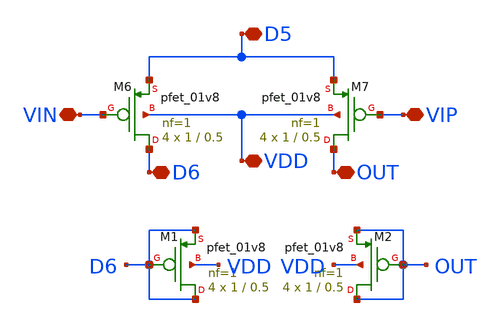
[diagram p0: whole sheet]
** sch_path: block3/xschem/block3.sch
**.subckt block3 D5 D6 VDD VIN VIP OUT
*.iopin D5
*.iopin D6
*.iopin VDD
*.iopin VIN
*.iopin VIP
*.iopin OUT
XM6 D6 VIN D5 VDD sky130_fd_pr__pfet_01v8 L=0.5 W=1 nf=1 ad='int((nf+1)/2) * W/nf * 0.29' as='int((nf+2)/2) * W/nf * 0.29'
+ pd='2*int((nf+1)/2) * (W/nf + 0.29)' ps='2*int((nf+2)/2) * (W/nf + 0.29)' nrd='0.29 / W' nrs='0.29 / W'
+ sa=0 sb=0 sd=0 mult=4 m=4
XM7 OUT VIP D5 VDD sky130_fd_pr__pfet_01v8 L=0.5 W=1 nf=1 ad='int((nf+1)/2) * W/nf * 0.29' as='int((nf+2)/2) * W/nf * 0.29'
+ pd='2*int((nf+1)/2) * (W/nf + 0.29)' ps='2*int((nf+2)/2) * (W/nf + 0.29)' nrd='0.29 / W' nrs='0.29 / W'
+ sa=0 sb=0 sd=0 mult=4 m=4
XM1 D6 D6 D6 VDD sky130_fd_pr__pfet_01v8 L=0.5 W=1 nf=1 ad='int((nf+1)/2) * W/nf * 0.29' as='int((nf+2)/2) * W/nf * 0.29'
+ pd='2*int((nf+1)/2) * (W/nf + 0.29)' ps='2*int((nf+2)/2) * (W/nf + 0.29)' nrd='0.29 / W' nrs='0.29 / W'
+ sa=0 sb=0 sd=0 mult=4 m=4
XM2 OUT OUT OUT VDD sky130_fd_pr__pfet_01v8 L=0.5 W=1 nf=1 ad='int((nf+1)/2) * W/nf * 0.29' as='int((nf+2)/2) * W/nf * 0.29'
+ pd='2*int((nf+1)/2) * (W/nf + 0.29)' ps='2*int((nf+2)/2) * (W/nf + 0.29)' nrd='0.29 / W' nrs='0.29 / W'
+ sa=0 sb=0 sd=0 mult=4 m=4
**.ends
.end
